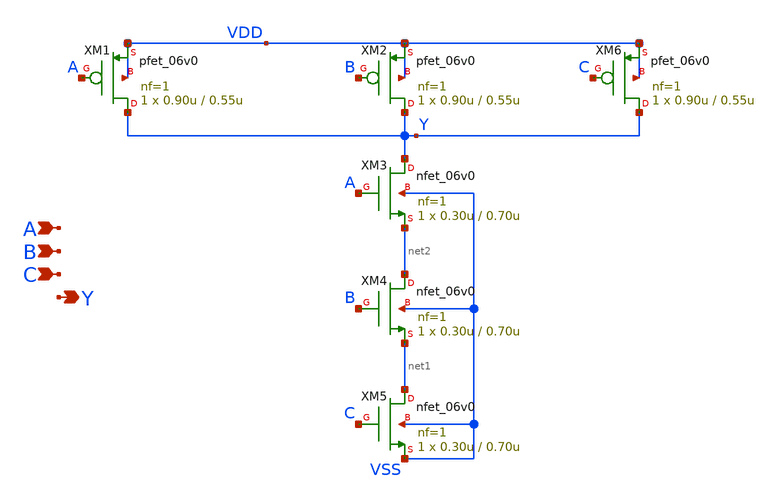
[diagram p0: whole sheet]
** sch_path: designs/libs/core_analog/digital/digital_nand3_1.sch
**.subckt digital_nand3_1 A B Y C
*.ipin A
*.ipin B
*.opin Y
*.ipin C
XM1 Y A VDD VDD pfet_06v0 L=0.55u W=0.90u nf=1 ad='int((nf+1)/2) * W/nf * 0.18u' as='int((nf+2)/2) * W/nf * 0.18u'
+ pd='2*int((nf+1)/2) * (W/nf + 0.18u)' ps='2*int((nf+2)/2) * (W/nf + 0.18u)' nrd='0.18u / W' nrs='0.18u / W'
+ sa=0 sb=0 sd=0 m=1
XM2 Y B VDD VDD pfet_06v0 L=0.55u W=0.90u nf=1 ad='int((nf+1)/2) * W/nf * 0.18u' as='int((nf+2)/2) * W/nf * 0.18u'
+ pd='2*int((nf+1)/2) * (W/nf + 0.18u)' ps='2*int((nf+2)/2) * (W/nf + 0.18u)' nrd='0.18u / W' nrs='0.18u / W'
+ sa=0 sb=0 sd=0 m=1
XM6 Y C VDD VDD pfet_06v0 L=0.55u W=0.90u nf=1 ad='int((nf+1)/2) * W/nf * 0.18u' as='int((nf+2)/2) * W/nf * 0.18u'
+ pd='2*int((nf+1)/2) * (W/nf + 0.18u)' ps='2*int((nf+2)/2) * (W/nf + 0.18u)' nrd='0.18u / W' nrs='0.18u / W'
+ sa=0 sb=0 sd=0 m=1
XM3 Y A net2 VSS nfet_06v0 L=0.70u W=0.30u nf=1 ad='int((nf+1)/2) * W/nf * 0.18u' as='int((nf+2)/2) * W/nf * 0.18u'
+ pd='2*int((nf+1)/2) * (W/nf + 0.18u)' ps='2*int((nf+2)/2) * (W/nf + 0.18u)' nrd='0.18u / W' nrs='0.18u / W'
+ sa=0 sb=0 sd=0 m=1
XM4 net2 B net1 VSS nfet_06v0 L=0.70u W=0.30u nf=1 ad='int((nf+1)/2) * W/nf * 0.18u' as='int((nf+2)/2) * W/nf * 0.18u'
+ pd='2*int((nf+1)/2) * (W/nf + 0.18u)' ps='2*int((nf+2)/2) * (W/nf + 0.18u)' nrd='0.18u / W' nrs='0.18u / W'
+ sa=0 sb=0 sd=0 m=1
XM5 net1 C VSS VSS nfet_06v0 L=0.70u W=0.30u nf=1 ad='int((nf+1)/2) * W/nf * 0.18u' as='int((nf+2)/2) * W/nf * 0.18u'
+ pd='2*int((nf+1)/2) * (W/nf + 0.18u)' ps='2*int((nf+2)/2) * (W/nf + 0.18u)' nrd='0.18u / W' nrs='0.18u / W'
+ sa=0 sb=0 sd=0 m=1
**.ends
.end
